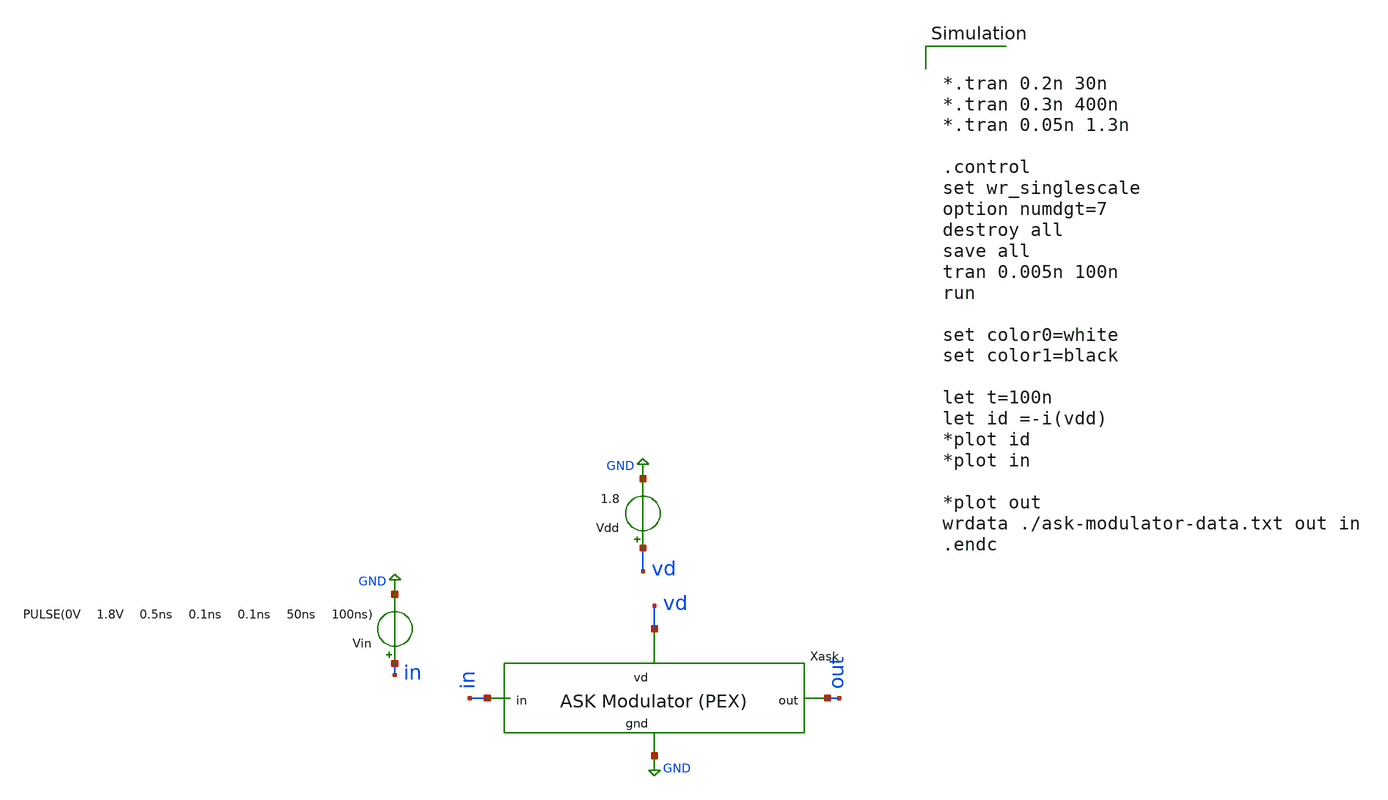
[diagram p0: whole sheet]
** sch_path: ask_modulator/xschem/ask-modulator_tb-tran.sch
**.subckt ask-modulator_tb-tran
Vdd vd GND 1.8
Vin in GND PULSE(0V 1.8V 0.5ns 0.1ns 0.1ns 50ns 100ns)
x1 vd out in GND ask-modulator-pex
**** begin user architecture code


*.tran 0.2n 30n
*.tran 0.3n 400n
*.tran 0.05n 1.3n

.control
set wr_singlescale
option numdgt=7
destroy all
save all
tran 0.005n 100n
run

set color0=white
set color1=black

let t=100n
let id =-i(vdd)
*plot id
*plot in

*plot out
wrdata ./ask-modulator-data.txt out in
.endc

 .lib $::SKYWATER_MODELS/sky130.lib.spice tt
.include $::SKYWATER_STDCELLS/sky130_fd_sc_hd.spice

**** end user architecture code
**.ends
.GLOBAL GND
.end
